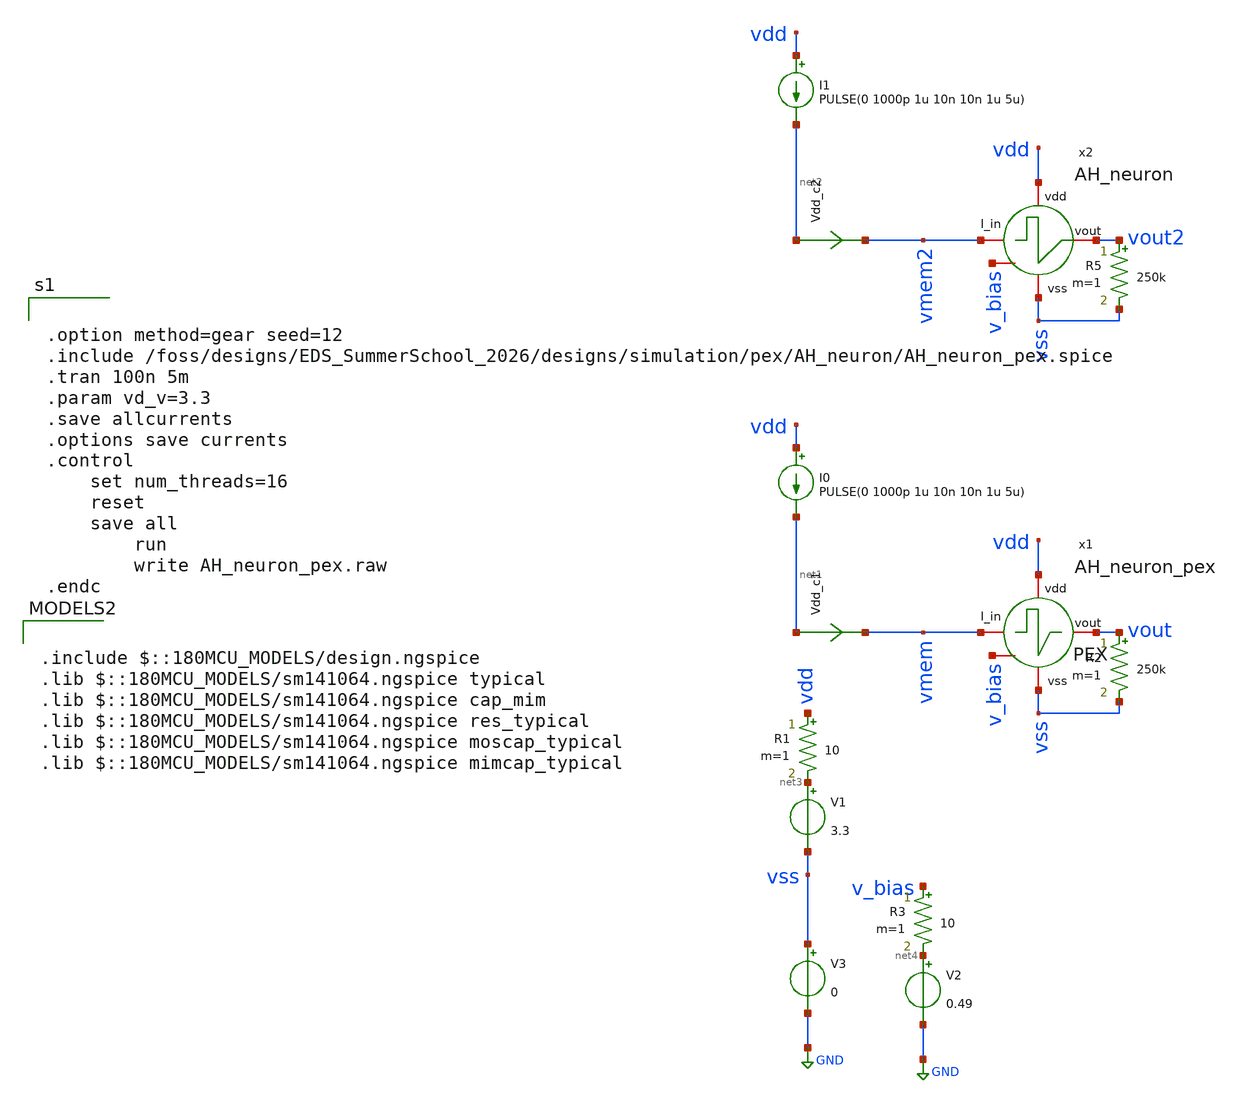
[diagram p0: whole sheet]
** sch_path: designs/simulation/pex/AH_neuron/AH_neuron_pex.sch
**.subckt AH_neuron_pex
V1 net3 vss 3.3
I0 vdd net1 PULSE(0 1000p 1u 10n 10n 1u 5u)
R1 vdd net3 10 m=1
R2 vout vss 250k m=1
Vdd_c1 net1 vmem 0
.save i(vdd_c1)
V2 net4 GND 0.49
R3 v_bias net4 10 m=1
V3 vss GND 0
x2 vdd vmem2 vout2 vss v_bias AH_neuron
I1 vdd net2 PULSE(0 1000p 1u 10n 10n 1u 5u)
R5 vout2 vss 250k m=1
Vdd_c2 net2 vmem2 0
.save i(vdd_c2)
x1 vdd vmem vout vss v_bias AH_neuron_pex
**** begin user architecture code


.option method=gear seed=12
.include /foss/designs/EDS_SummerSchool_2026/designs/simulation/pex/AH_neuron/AH_neuron_pex.spice
.tran 100n 5m
.param vd_v=3.3
.save allcurrents
.options save currents
.control
	set num_threads=16
	reset
	save all
        run
        write AH_neuron_pex.raw
.endc



.include $::180MCU_MODELS/design.ngspice
.lib $::180MCU_MODELS/sm141064.ngspice typical
.lib $::180MCU_MODELS/sm141064.ngspice cap_mim
.lib $::180MCU_MODELS/sm141064.ngspice res_typical
.lib $::180MCU_MODELS/sm141064.ngspice moscap_typical
.lib $::180MCU_MODELS/sm141064.ngspice mimcap_typical

**** end user architecture code
**.ends
.GLOBAL GND
.end
